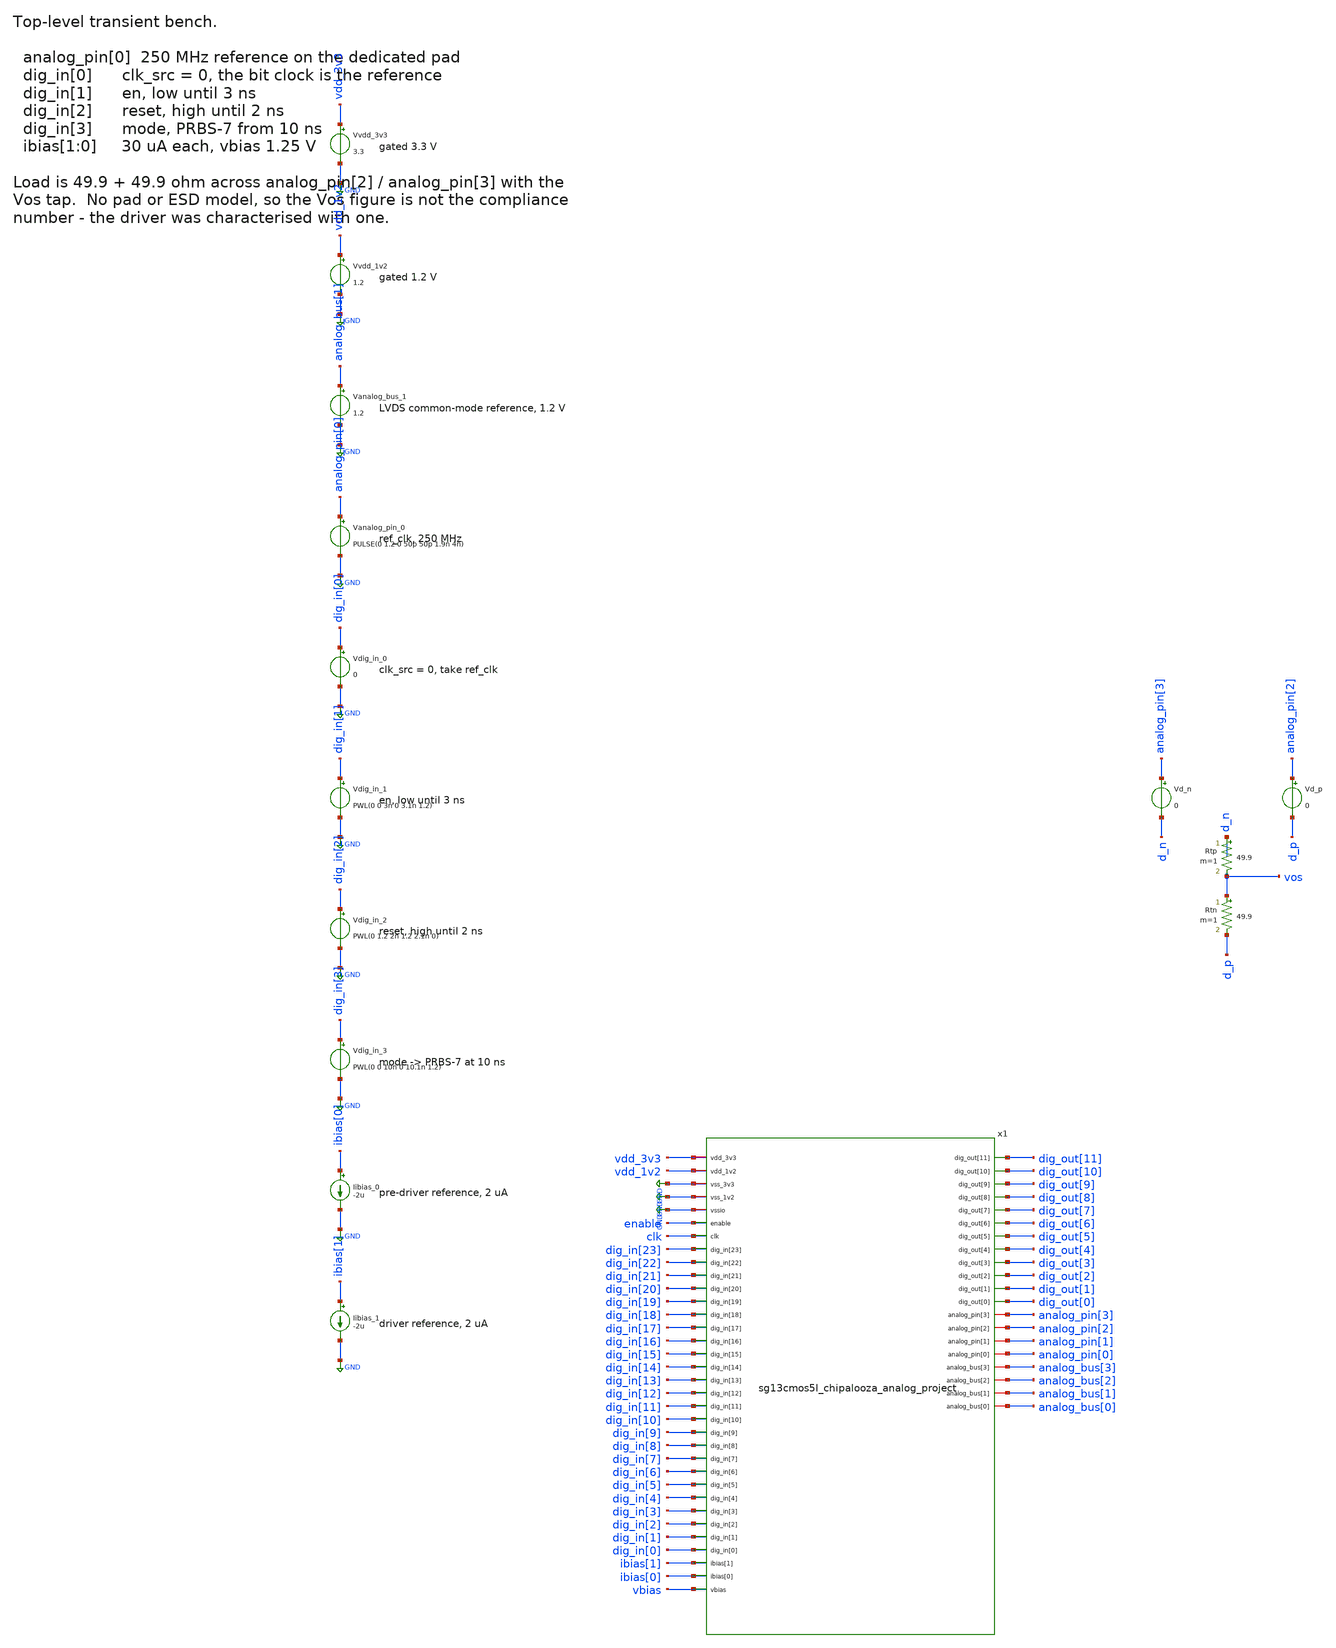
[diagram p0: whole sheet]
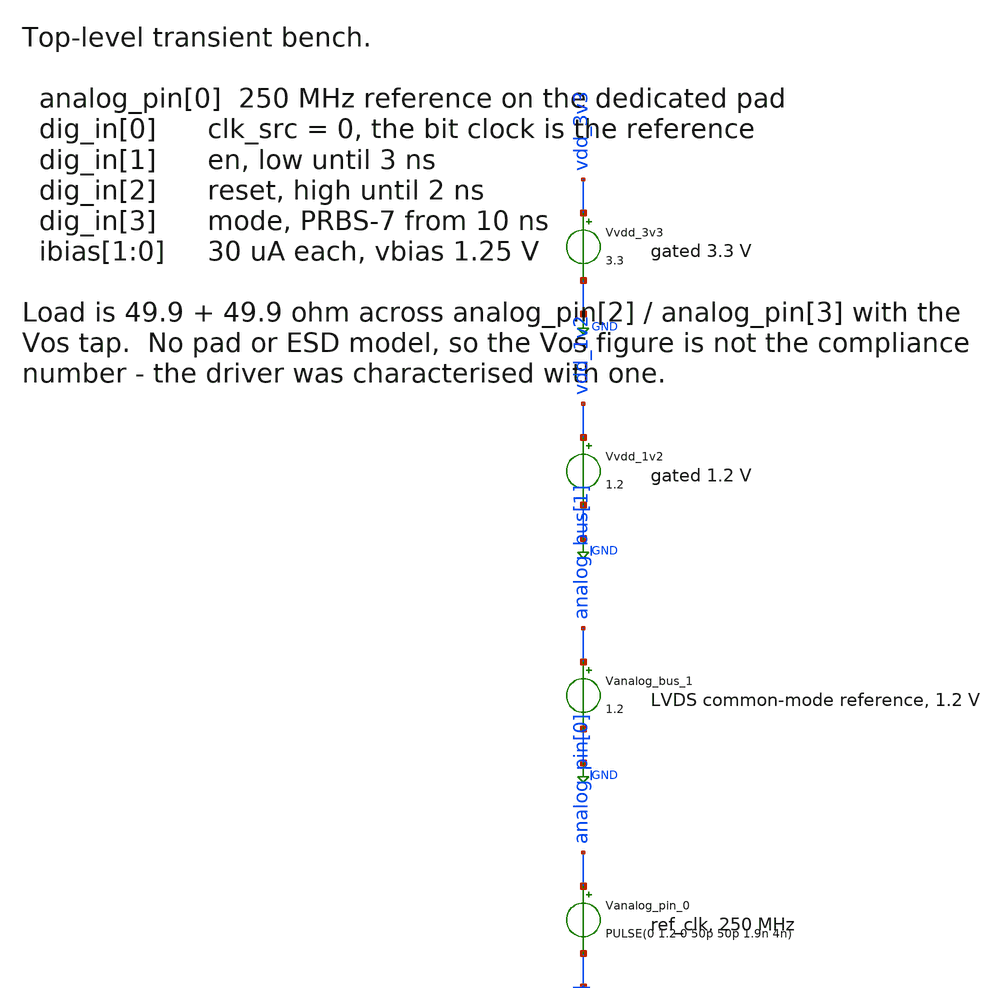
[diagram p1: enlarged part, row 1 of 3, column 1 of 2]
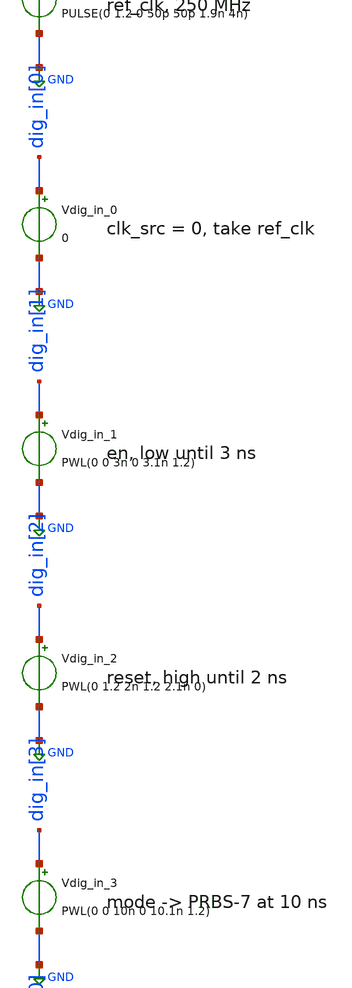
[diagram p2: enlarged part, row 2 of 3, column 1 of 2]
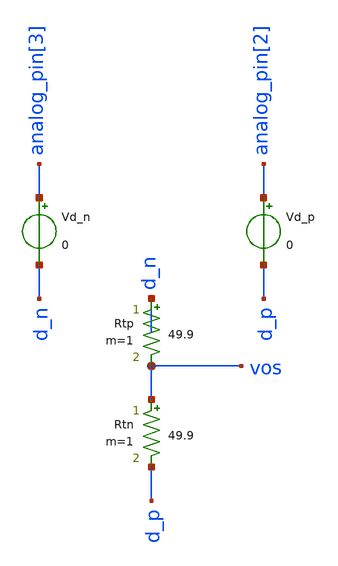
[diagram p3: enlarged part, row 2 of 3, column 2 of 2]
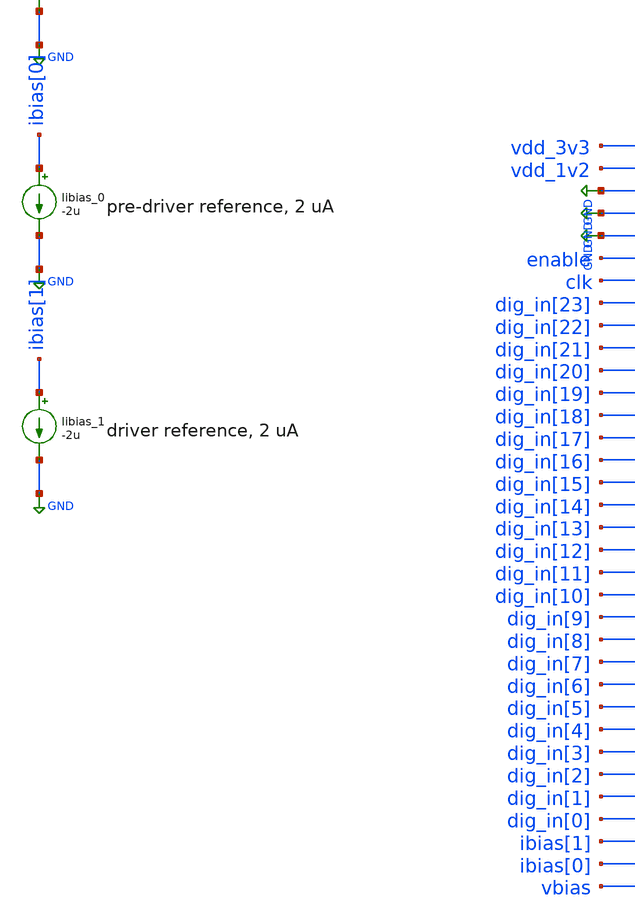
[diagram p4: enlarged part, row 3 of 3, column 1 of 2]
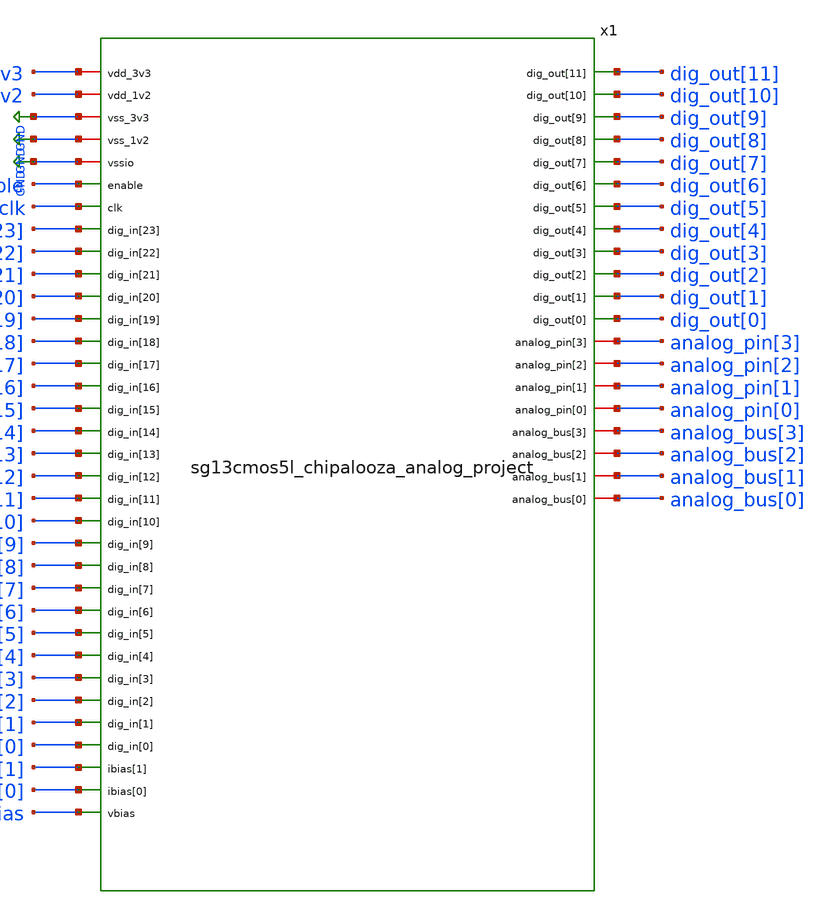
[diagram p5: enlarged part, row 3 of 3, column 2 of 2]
** sch_path: testbenches/xschem/sg13cmos5l_chipalooza_analog_project_tb_tran.sch
**.subckt sg13cmos5l_chipalooza_analog_project_tb_tran
Vvdd_3v3 vdd_3v3 GND 3.3
Vvdd_1v2 vdd_1v2 GND 1.2
Vanalog_bus_1 analog_bus[1] GND 1.2
Vanalog_pin_0 analog_pin[0] GND PULSE(0 1.2 0 50p 50p 1.9n 4n)
Vdig_in_0 dig_in[0] GND 0
Vdig_in_1 dig_in[1] GND PWL(0 0 3n 0 3.1n 1.2)
Vdig_in_2 dig_in[2] GND PWL(0 1.2 2n 1.2 2.1n 0)
Vdig_in_3 dig_in[3] GND PWL(0 0 10n 0 10.1n 1.2)
Iibias_0 ibias[0] GND -2u
Iibias_1 ibias[1] GND -2u
x1 vdd_3v3 vdd_1v2 GND GND GND enable clk dig_in[23] dig_in[22] dig_in[21] dig_in[20] dig_in[19]
+ dig_in[18] dig_in[17] dig_in[16] dig_in[15] dig_in[14] dig_in[13] dig_in[12] dig_in[11] dig_in[10] dig_in[9]
+ dig_in[8] dig_in[7] dig_in[6] dig_in[5] dig_in[4] dig_in[3] dig_in[2] dig_in[1] dig_in[0] ibias[1] ibias[0]
+ vbias dig_out[11] dig_out[10] dig_out[9] dig_out[8] dig_out[7] dig_out[6] dig_out[5] dig_out[4]
+ dig_out[3] dig_out[2] dig_out[1] dig_out[0] analog_pin[3] analog_pin[2] analog_pin[1] analog_pin[0]
+ analog_bus[3] analog_bus[2] analog_bus[1] analog_bus[0] sg13cmos5l_chipalooza_analog_project
Vd_n analog_pin[3] d_n 0
Vd_p analog_pin[2] d_p 0
Rtp d_n vos 49.9 m=1
Rtn vos d_p 49.9 m=1
**** begin user architecture code


.lib cornerMOSlv.lib mos_tt
.lib cornerMOShv.lib mos_tt
.lib cornerRES.lib res_typ
.lib cornerDIO.lib dio_tt
.include cap_cmomf.lib
.include /foss/pdks/ihp-sg13cmos5l/libs.ref/sg13cmos5l_stdcell/spice/sg13cmos5l_stdcell.spice
.temp 27
* gear2 collapses the timestep to 6e-24 s at 414 ns on vvdd_1v2#branch
* once the PLL's XSPICE bridges are in the netlist, and the run stops
* there whatever tstop says.  trap gets through the full span.
.options savecurrents klu method=trap reltol=1e-3 abstol=1e-12 gmin=1e-12
.control
* The top cell carries pll_cosim, whose RTL half only couples to the analog
* loop once ngspice holds the auto-bridge templates.  Those are injected into
* the netlist after xschem writes it, by scripts/pll/inject_cosim_bridges.py,
* because the quotes their syntax needs would end xschem's value=... property
* and silently take .endc with them.
*
* make sim-xschem netlists, injects, then simulates.  The Simulate arrow in
* xschem does not netlist - it runs ngspice on whatever netlist is already
* there, so it works after a make run and fails after xschem has written a
* fresh one.  Without the bridges nothing couples and every waveform comes
* out flat, so stop here rather than produce a plausible-looking lie.
if $?auto_bridge_d_in = 0
  echo
  echo ERROR: d_cosim auto-bridges are not set, so the PLL is disconnected.
  echo Fix: run make sim-xschem with the TB= name of this bench.
  echo The Simulate arrow reuses that netlist afterwards and will work.
  echo
* quit 1 rather than quit: xschem runs ngspice in a terminal that falls back
* to a shell only on a non-zero exit.  Quitting with zero closes the window
* before the message above can be read.
  quit 1
end
* xpll is pll_cosim: the PFD and both dividers are the RTL of
* macros/pll_digital, through d_cosim.  The analog/digital bridges are
* inserted into the netlist by scripts/pll/inject_cosim_bridges.py - they
* cannot live here: xschem ends the value property at the first quote.
* Build the shared object first: make pll-cosim-so.
save all
op
remzerovec
write @schname\.raw
set appendwrite
tran 5p 40n
write @schname\.raw

let vod = v(d_p)-v(d_n)
meas tran vod_max MAX vod from=20n to=40n
meas tran vod_min MIN vod from=20n to=40n
meas tran vos_avg AVG v(vos) from=20n to=40n
meas tran vos_max MAX v(vos) from=20n to=40n
meas tran vos_min MIN v(vos) from=20n to=40n
let vos_pp = vos_max - vos_min
print vod_max vod_min vos_avg vos_pp

set wr_vecnames
set wr_singlescale
wrdata ../plot_simulations/data/@schname\.txt  v(d_p) v(d_n) v(vos) vod v(x1.core_p) v(x1.core_n)
.endc


**** end user architecture code
**.ends
.GLOBAL GND
.end
